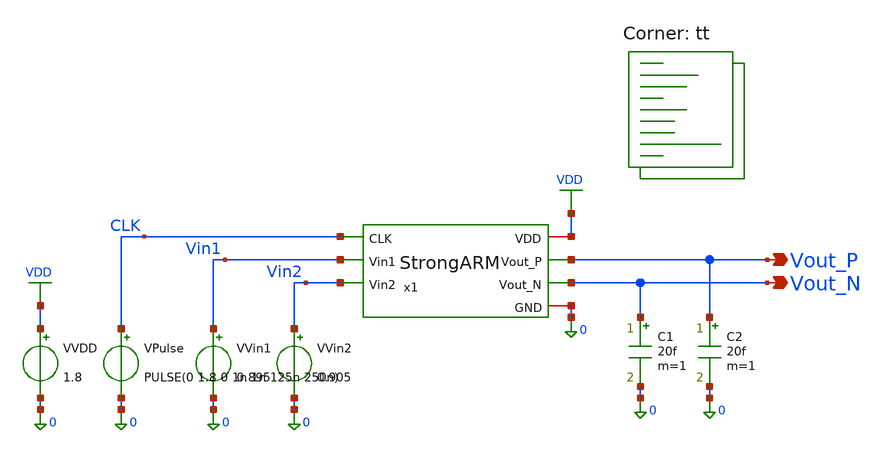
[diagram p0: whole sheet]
** sch_path: blocks/03_StrongARM/sim/tb_StrongARM_Power.sch
**.subckt tb_StrongARM_Power Vout_P Vout_N
*.opin Vout_P
*.opin Vout_N
x1 VDD CLK Vout_P Vout_N Vin1 Vin2 0 StrongARM
VVDD VDD 0 1.8
VVin1 Vin1 0 0.895
VVin2 Vin2 0 0.905
VPulse CLK 0 PULSE(0 1.8 0 1n 1n 125n 250n)
C1 Vout_N 0 20f m=1
C2 Vout_P 0 20f m=1
**** begin user architecture code



.control
save all

* ===================================
* BLOCK 3 - STRONGARM COMPARATOR
* TEST 7A - POWER CHARACTERIZATION
* VDD = 1.8 V
* CLK = 4 MHz
* CORNER = tt
* ===================================

tran 0.2n 2.5u

* Ignore startup period
* Measure supply current over 8 cycles
meas tran ivdd_avg AVG i(VVDD) FROM=500n TO=2.5u

* Calculate average power
let p_avg = -1.8 * ivdd_avg

* One comparator decision per cycle
let e_decision = p_avg / 4e6

echo =============================
echo TEST 7A - POWER RESULTS
echo =============================

print ivdd_avg
print p_avg
print e_decision

echo =============================
echo OUTPUT VOLTAGE LIMITS
echo =============================

meas tran vp_max MAX v(vout_p) FROM=500n TO=2.5u
meas tran vp_min MIN v(vout_p) FROM=500n TO=2.5u

meas tran vn_max MAX v(vout_n) FROM=500n TO=2.5u
meas tran vn_min MIN v(vout_n) FROM=500n TO=2.5u

.endc

.lib $::SKYWATER_MODELS/sky130.lib.spice tt
**** end user architecture code
**.ends

* expanding   symbol:  blocks/03_StrongARM/xschem/StrongARM.sym # of pins=7
** sym_path: blocks/03_StrongARM/xschem/StrongARM.sym
** sch_path: blocks/03_StrongARM/xschem/StrongARM.sch
.subckt StrongARM VDD CLK Vout_P Vout_N Vin1 Vin2 GND
*.iopin VDD
*.iopin GND
*.ipin Vin1
*.ipin Vin2
*.ipin CLK
*.opin Vout_P
*.opin Vout_N
XS1 P CLK VDD VDD sky130_fd_pr__pfet_01v8 L=0.15 W=1.5 nf=1 ad='int((1 + 1)/2) * 1.5 / 1 * 0.29' as='int((1 + 2)/2) * 1.5 / 1 * 0.29'
+ pd='2*int((1 + 1)/2) * (1.5 / 1 + 0.29)' ps='2*int((1 + 2)/2) * (1.5 / 1 + 0.29)' nrd='0.29 / 1.5 ' nrs='0.29 / 1.5 '
+ sa=0 sb=0 sd=0 mult=1 m=1
XS3 Vout_P CLK VDD VDD sky130_fd_pr__pfet_01v8 L=0.15 W=1.5 nf=1 ad='int((1 + 1)/2) * 1.5 / 1 * 0.29'
+ as='int((1 + 2)/2) * 1.5 / 1 * 0.29' pd='2*int((1 + 1)/2) * (1.5 / 1 + 0.29)' ps='2*int((1 + 2)/2) * (1.5 / 1 + 0.29)'
+ nrd='0.29 / 1.5 ' nrs='0.29 / 1.5 ' sa=0 sb=0 sd=0 mult=1 m=1
XM5 Vout_P Vout_N VDD VDD sky130_fd_pr__pfet_01v8 L=0.3 W=5 nf=1 ad='int((1 + 1)/2) * 5 / 1 * 0.29' as='int((1 + 2)/2) * 5 / 1 * 0.29'
+ pd='2*int((1 + 1)/2) * (5 / 1 + 0.29)' ps='2*int((1 + 2)/2) * (5 / 1 + 0.29)' nrd='0.29 / 5 ' nrs='0.29 / 5 '
+ sa=0 sb=0 sd=0 mult=1 m=1
XM6 Vout_N Vout_P VDD VDD sky130_fd_pr__pfet_01v8 L=0.3 W=5 nf=1 ad='int((1 + 1)/2) * 5 / 1 * 0.29' as='int((1 + 2)/2) * 5 / 1 * 0.29'
+ pd='2*int((1 + 1)/2) * (5 / 1 + 0.29)' ps='2*int((1 + 2)/2) * (5 / 1 + 0.29)' nrd='0.29 / 5 ' nrs='0.29 / 5 '
+ sa=0 sb=0 sd=0 mult=1 m=1
XS4 Vout_N CLK VDD VDD sky130_fd_pr__pfet_01v8 L=0.15 W=1.5 nf=1 ad='int((1 + 1)/2) * 1.5 / 1 * 0.29'
+ as='int((1 + 2)/2) * 1.5 / 1 * 0.29' pd='2*int((1 + 1)/2) * (1.5 / 1 + 0.29)' ps='2*int((1 + 2)/2) * (1.5 / 1 + 0.29)'
+ nrd='0.29 / 1.5 ' nrs='0.29 / 1.5 ' sa=0 sb=0 sd=0 mult=1 m=1
XS2 Q CLK VDD VDD sky130_fd_pr__pfet_01v8 L=0.15 W=1.5 nf=1 ad='int((1 + 1)/2) * 1.5 / 1 * 0.29' as='int((1 + 2)/2) * 1.5 / 1 * 0.29'
+ pd='2*int((1 + 1)/2) * (1.5 / 1 + 0.29)' ps='2*int((1 + 2)/2) * (1.5 / 1 + 0.29)' nrd='0.29 / 1.5 ' nrs='0.29 / 1.5 '
+ sa=0 sb=0 sd=0 mult=1 m=1
XM3 Vout_P Vout_N P GND sky130_fd_pr__nfet_01v8 L=0.3 W=2 nf=1 ad='int((1 + 1)/2) * 2 / 1 * 0.29' as='int((1 + 2)/2) * 2 / 1 * 0.29'
+ pd='2*int((1 + 1)/2) * (2 / 1 + 0.29)' ps='2*int((1 + 2)/2) * (2 / 1 + 0.29)' nrd='0.29 / 2 ' nrs='0.29 / 2 '
+ sa=0 sb=0 sd=0 mult=1 m=1
XM4 Vout_N Vout_P Q GND sky130_fd_pr__nfet_01v8 L=0.3 W=2 nf=1 ad='int((1 + 1)/2) * 2 / 1 * 0.29' as='int((1 + 2)/2) * 2 / 1 * 0.29'
+ pd='2*int((1 + 1)/2) * (2 / 1 + 0.29)' ps='2*int((1 + 2)/2) * (2 / 1 + 0.29)' nrd='0.29 / 2 ' nrs='0.29 / 2 '
+ sa=0 sb=0 sd=0 mult=1 m=1
XM1 P Vin1 TAIL GND sky130_fd_pr__nfet_01v8 L=0.5 W=10 nf=1 ad='int((1 + 1)/2) * 10 / 1 * 0.29' as='int((1 + 2)/2) * 10 / 1 * 0.29'
+ pd='2*int((1 + 1)/2) * (10 / 1 + 0.29)' ps='2*int((1 + 2)/2) * (10 / 1 + 0.29)' nrd='0.29 / 10 ' nrs='0.29 / 10 '
+ sa=0 sb=0 sd=0 mult=1 m=1
XM2 Q Vin2 TAIL GND sky130_fd_pr__nfet_01v8 L=0.5 W=10 nf=1 ad='int((1 + 1)/2) * 10 / 1 * 0.29' as='int((1 + 2)/2) * 10 / 1 * 0.29'
+ pd='2*int((1 + 1)/2) * (10 / 1 + 0.29)' ps='2*int((1 + 2)/2) * (10 / 1 + 0.29)' nrd='0.29 / 10 ' nrs='0.29 / 10 '
+ sa=0 sb=0 sd=0 mult=1 m=1
XM7 TAIL CLK GND GND sky130_fd_pr__nfet_01v8 L=0.3 W=1 nf=1 ad='int((1 + 1)/2) * 1 / 1 * 0.29' as='int((1 + 2)/2) * 1 / 1 * 0.29'
+ pd='2*int((1 + 1)/2) * (1 / 1 + 0.29)' ps='2*int((1 + 2)/2) * (1 / 1 + 0.29)' nrd='0.29 / 1 ' nrs='0.29 / 1 '
+ sa=0 sb=0 sd=0 mult=1 m=1
.ends

.GLOBAL VDD
.end
